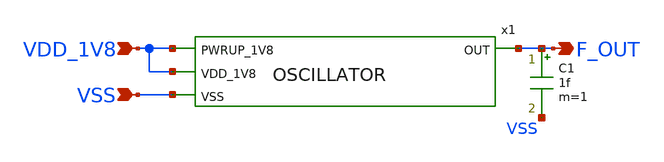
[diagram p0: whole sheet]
** sch_path: design/LELO_GR03_SKY130A/OSCILLATOR_TB.sch
**.subckt OSCILLATOR_TB VDD_1V8 F_OUT VSS
*.ipin VDD_1V8
*.opin F_OUT
*.ipin VSS
x1 VDD_1V8 F_OUT VDD_1V8 VSS OSCILLATOR
C1 F_OUT VSS 1f m=1
**.ends
.end
